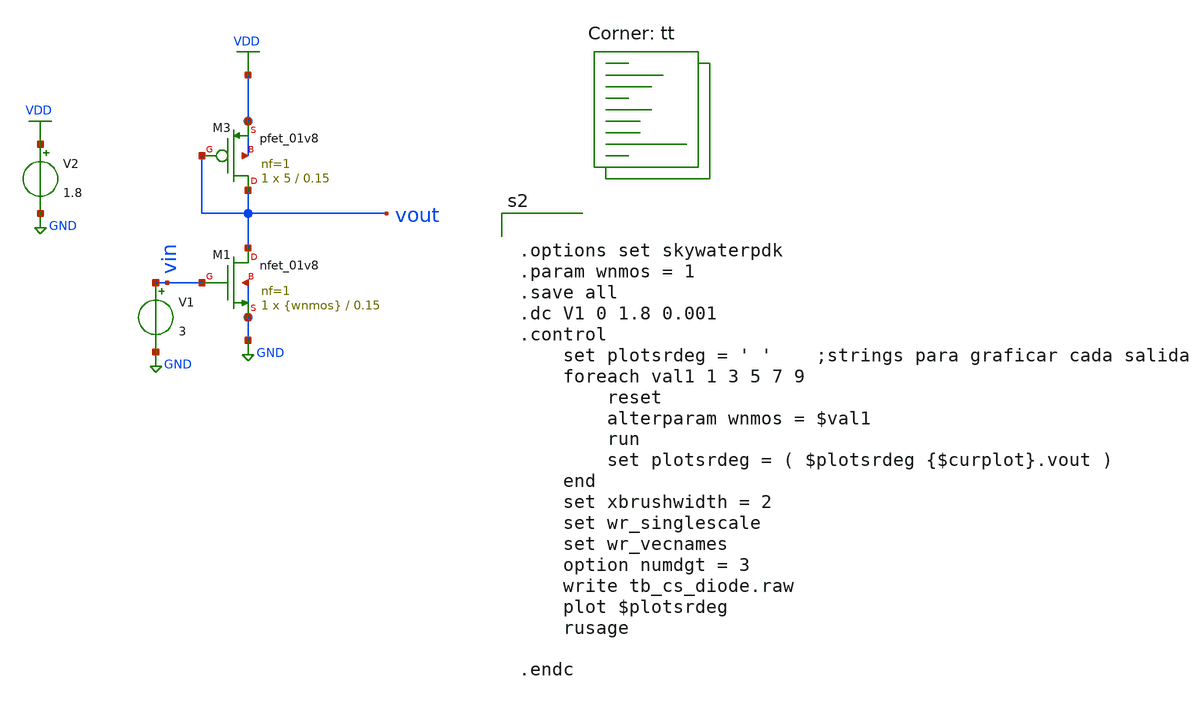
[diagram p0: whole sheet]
** sch_path: VCCS/tb_cs_diode.sch
**.subckt tb_cs_diode
XM1 vout vin GND GND sky130_fd_pr__nfet_01v8 L=0.15 W={wnmos} nf=1 ad='int((1 + 1)/2) * {wnmos} / 1 * 0.29'
+ as='int((1 + 2)/2) * {wnmos} / 1 * 0.29' pd='2*int((1 + 1)/2) * ({wnmos} / 1 + 0.29)' ps='2*int((1 + 2)/2) * ({wnmos} / 1 + 0.29)'
+ nrd='0.29 / {wnmos} ' nrs='0.29 / {wnmos} ' sa=0 sb=0 sd=0 mult=1 m=1
XM3 vout vout VDD VDD sky130_fd_pr__pfet_01v8 L=0.15 W=5 nf=1 ad='int((1 + 1)/2) * 5 / 1 * 0.29' as='int((1 + 2)/2) * 5 / 1 * 0.29'
+ pd='2*int((1 + 1)/2) * (5 / 1 + 0.29)' ps='2*int((1 + 2)/2) * (5 / 1 + 0.29)' nrd='0.29 / 5 ' nrs='0.29 / 5 '
+ sa=0 sb=0 sd=0 mult=1 m=1
V1 vin GND 3
V2 VDD GND 1.8
**** begin user architecture code
.lib $::SKYWATER_MODELS/sky130.lib.spice tt


.options set skywaterpdk
.param wnmos = 1
.save all
.dc V1 0 1.8 0.001
.control
	set plotsrdeg = ' '	;strings para graficar cada salida
	foreach val1 1 3 5 7 9
		reset
		alterparam wnmos = $val1
		run
		set plotsrdeg = ( $plotsrdeg {$curplot}.vout )
	end
	set xbrushwidth = 2
	set wr_singlescale
	set wr_vecnames
	option numdgt = 3
	write tb_cs_diode.raw
	plot $plotsrdeg
	rusage

.endc


**** end user architecture code
**.ends
.GLOBAL GND
.GLOBAL VDD
.end
